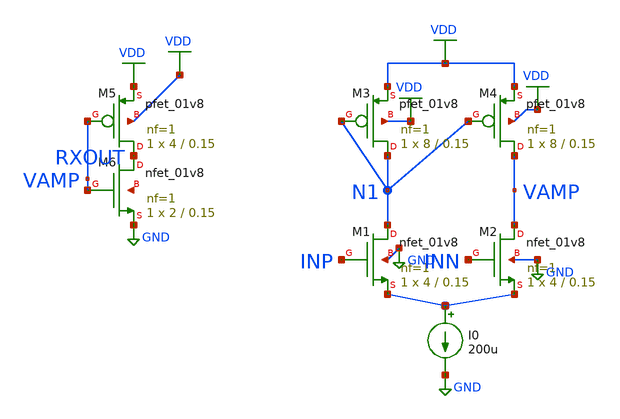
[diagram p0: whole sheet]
** sch_path: analog/rx_frontend.sch
**.subckt rx_frontend
XM1 N1 INP net1 GND sky130_fd_pr__nfet_01v8 L=0.15 W=4 nf=1 ad='int((1 + 1)/2) * 4 / 1 * 0.29' as='int((1 + 2)/2) * 4 / 1 * 0.29'
+ pd='2*int((1 + 1)/2) * (4 / 1 + 0.29)' ps='2*int((1 + 2)/2) * (4 / 1 + 0.29)' nrd='0.29 / 4 ' nrs='0.29 / 4 '
+ sa=0 sb=0 sd=0 mult=1 m=1
XM2 VAMP INN net1 GND sky130_fd_pr__nfet_01v8 L=0.15 W=4 nf=1 ad='int((1 + 1)/2) * 4 / 1 * 0.29' as='int((1 + 2)/2) * 4 / 1 * 0.29'
+ pd='2*int((1 + 1)/2) * (4 / 1 + 0.29)' ps='2*int((1 + 2)/2) * (4 / 1 + 0.29)' nrd='0.29 / 4 ' nrs='0.29 / 4 '
+ sa=0 sb=0 sd=0 mult=1 m=1
XM3 N1 N1 VDD VDD sky130_fd_pr__pfet_01v8 L=0.15 W=8 nf=1 ad='int((1 + 1)/2) * 8 / 1 * 0.29' as='int((1 + 2)/2) * 8 / 1 * 0.29'
+ pd='2*int((1 + 1)/2) * (8 / 1 + 0.29)' ps='2*int((1 + 2)/2) * (8 / 1 + 0.29)' nrd='0.29 / 8 ' nrs='0.29 / 8 '
+ sa=0 sb=0 sd=0 mult=1 m=1
XM4 VAMP N1 VDD VDD sky130_fd_pr__pfet_01v8 L=0.15 W=8 nf=1 ad='int((1 + 1)/2) * 8 / 1 * 0.29' as='int((1 + 2)/2) * 8 / 1 * 0.29'
+ pd='2*int((1 + 1)/2) * (8 / 1 + 0.29)' ps='2*int((1 + 2)/2) * (8 / 1 + 0.29)' nrd='0.29 / 8 ' nrs='0.29 / 8 '
+ sa=0 sb=0 sd=0 mult=1 m=1
XM6 RXOUT VAMP GND net2 sky130_fd_pr__nfet_01v8 L=0.15 W=2 nf=1 ad='int((1 + 1)/2) * 2 / 1 * 0.29' as='int((1 + 2)/2) * 2 / 1 * 0.29'
+ pd='2*int((1 + 1)/2) * (2 / 1 + 0.29)' ps='2*int((1 + 2)/2) * (2 / 1 + 0.29)' nrd='0.29 / 2 ' nrs='0.29 / 2 '
+ sa=0 sb=0 sd=0 mult=1 m=1
XM5 RXOUT VAMP VDD VDD sky130_fd_pr__pfet_01v8 L=0.15 W=4 nf=1 ad='int((1 + 1)/2) * 4 / 1 * 0.29' as='int((1 + 2)/2) * 4 / 1 * 0.29'
+ pd='2*int((1 + 1)/2) * (4 / 1 + 0.29)' ps='2*int((1 + 2)/2) * (4 / 1 + 0.29)' nrd='0.29 / 4 ' nrs='0.29 / 4 '
+ sa=0 sb=0 sd=0 mult=1 m=1
I0 net1 GND 200u
**.ends
.GLOBAL VDD
.GLOBAL GND
.end
